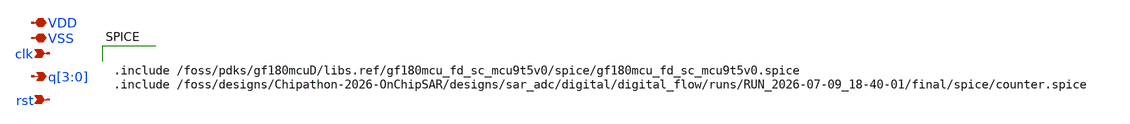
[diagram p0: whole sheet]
** sch_path: designs/sar_adc/digital/digital_flow/counter/counter.sch
**.subckt counter rst clk q[3],q[2],q[1],q[0] VDD VSS
*.ipin rst
*.ipin clk
*.opin q[3],q[2],q[1],q[0]
*.iopin VDD
*.iopin VSS
**** begin user architecture code

.include /foss/pdks/gf180mcuD/libs.ref/gf180mcu_fd_sc_mcu9t5v0/spice/gf180mcu_fd_sc_mcu9t5v0.spice
.include /foss/designs/Chipathon-2026-OnChipSAR/designs/sar_adc/digital/digital_flow/runs/RUN_2026-07-09_18-40-01/final/spice/counter.spice

**** end user architecture code
**.ends
.end
